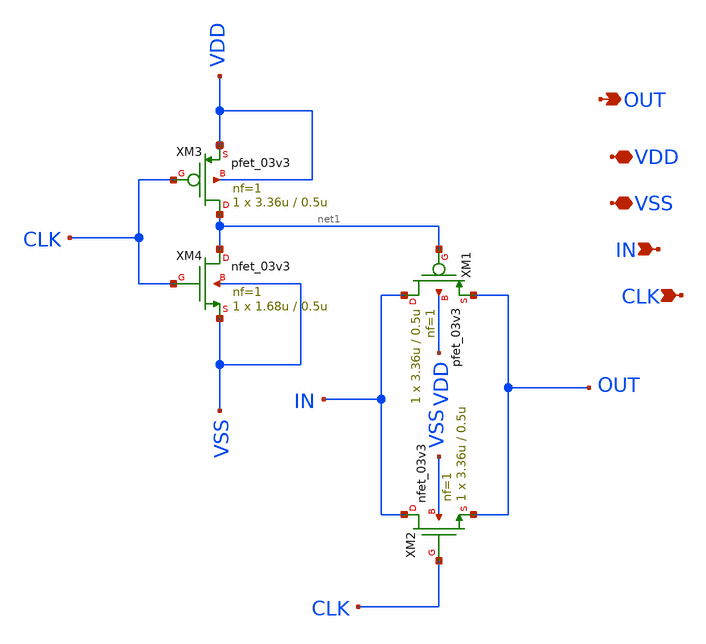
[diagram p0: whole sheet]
** sch_path: PLL-main/schematic/xschem/TR_Gate.sch
**.subckt TR_Gate VDD VSS IN OUT CLK
*.iopin VDD
*.iopin VSS
*.ipin IN
*.opin OUT
*.ipin CLK
XM1 IN net1 OUT VDD pfet_03v3 L=0.5u W=3.36u nf=1 ad='int((nf+1)/2) * W/nf * 0.18u' as='int((nf+2)/2) * W/nf * 0.18u'
+ pd='2*int((nf+1)/2) * (W/nf + 0.18u)' ps='2*int((nf+2)/2) * (W/nf + 0.18u)' nrd='0.18u / W' nrs='0.18u / W'
+ sa=0 sb=0 sd=0 m=1
XM2 IN CLK OUT VSS nfet_03v3 L=0.5u W=3.36u nf=1 ad='int((nf+1)/2) * W/nf * 0.18u' as='int((nf+2)/2) * W/nf * 0.18u'
+ pd='2*int((nf+1)/2) * (W/nf + 0.18u)' ps='2*int((nf+2)/2) * (W/nf + 0.18u)' nrd='0.18u / W' nrs='0.18u / W'
+ sa=0 sb=0 sd=0 m=1
XM3 net1 CLK VDD VDD pfet_03v3 L=0.5u W=3.36u nf=1 ad='int((nf+1)/2) * W/nf * 0.18u' as='int((nf+2)/2) * W/nf * 0.18u'
+ pd='2*int((nf+1)/2) * (W/nf + 0.18u)' ps='2*int((nf+2)/2) * (W/nf + 0.18u)' nrd='0.18u / W' nrs='0.18u / W'
+ sa=0 sb=0 sd=0 m=1
XM4 net1 CLK VSS VSS nfet_03v3 L=0.5u W=1.68u nf=1 ad='int((nf+1)/2) * W/nf * 0.18u' as='int((nf+2)/2) * W/nf * 0.18u'
+ pd='2*int((nf+1)/2) * (W/nf + 0.18u)' ps='2*int((nf+2)/2) * (W/nf + 0.18u)' nrd='0.18u / W' nrs='0.18u / W'
+ sa=0 sb=0 sd=0 m=1
**.ends
.end
